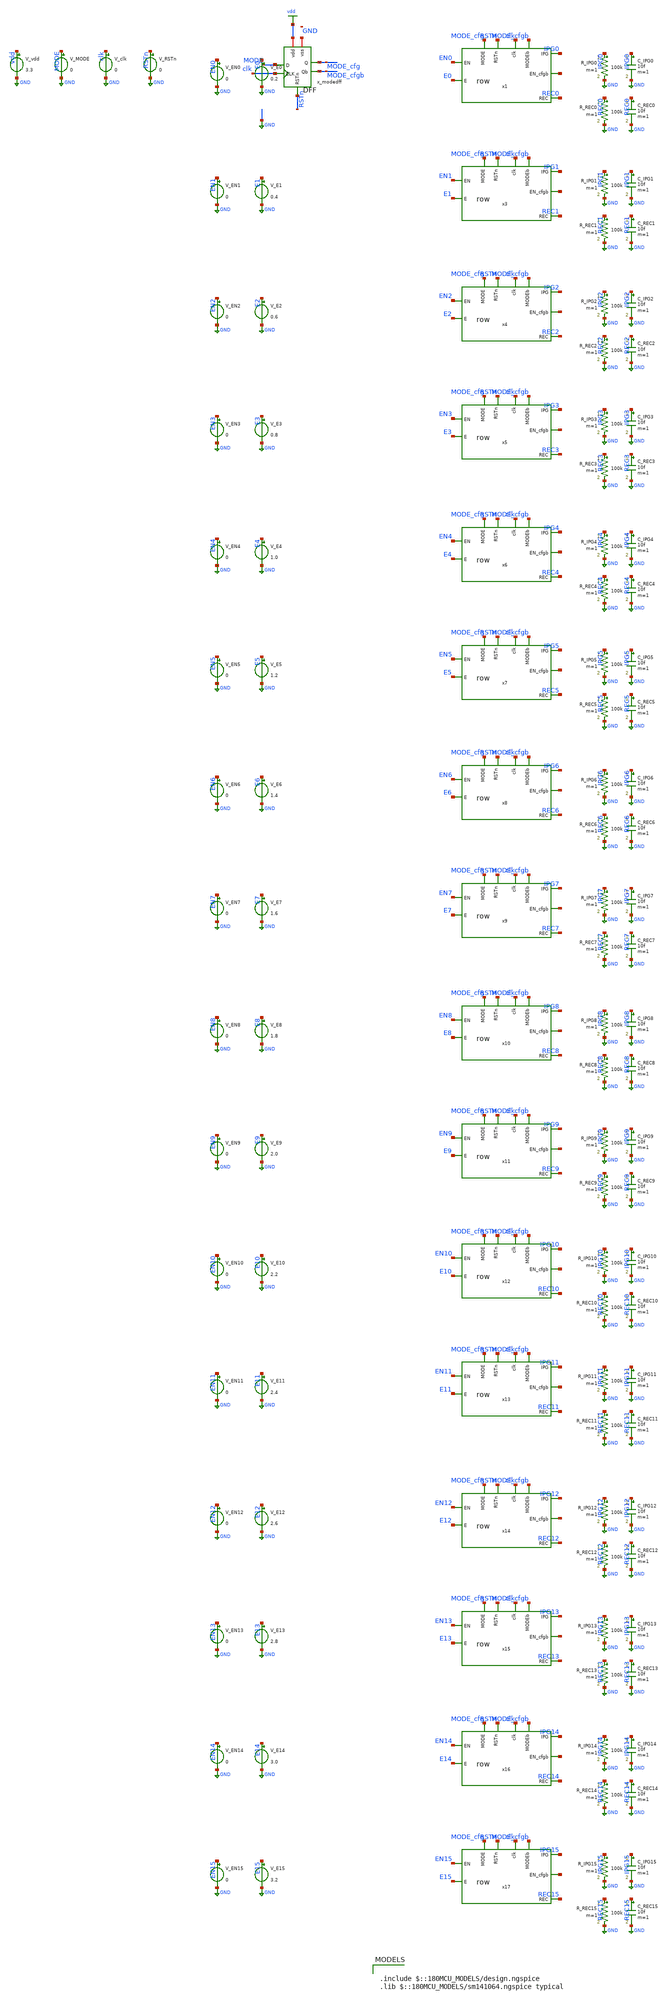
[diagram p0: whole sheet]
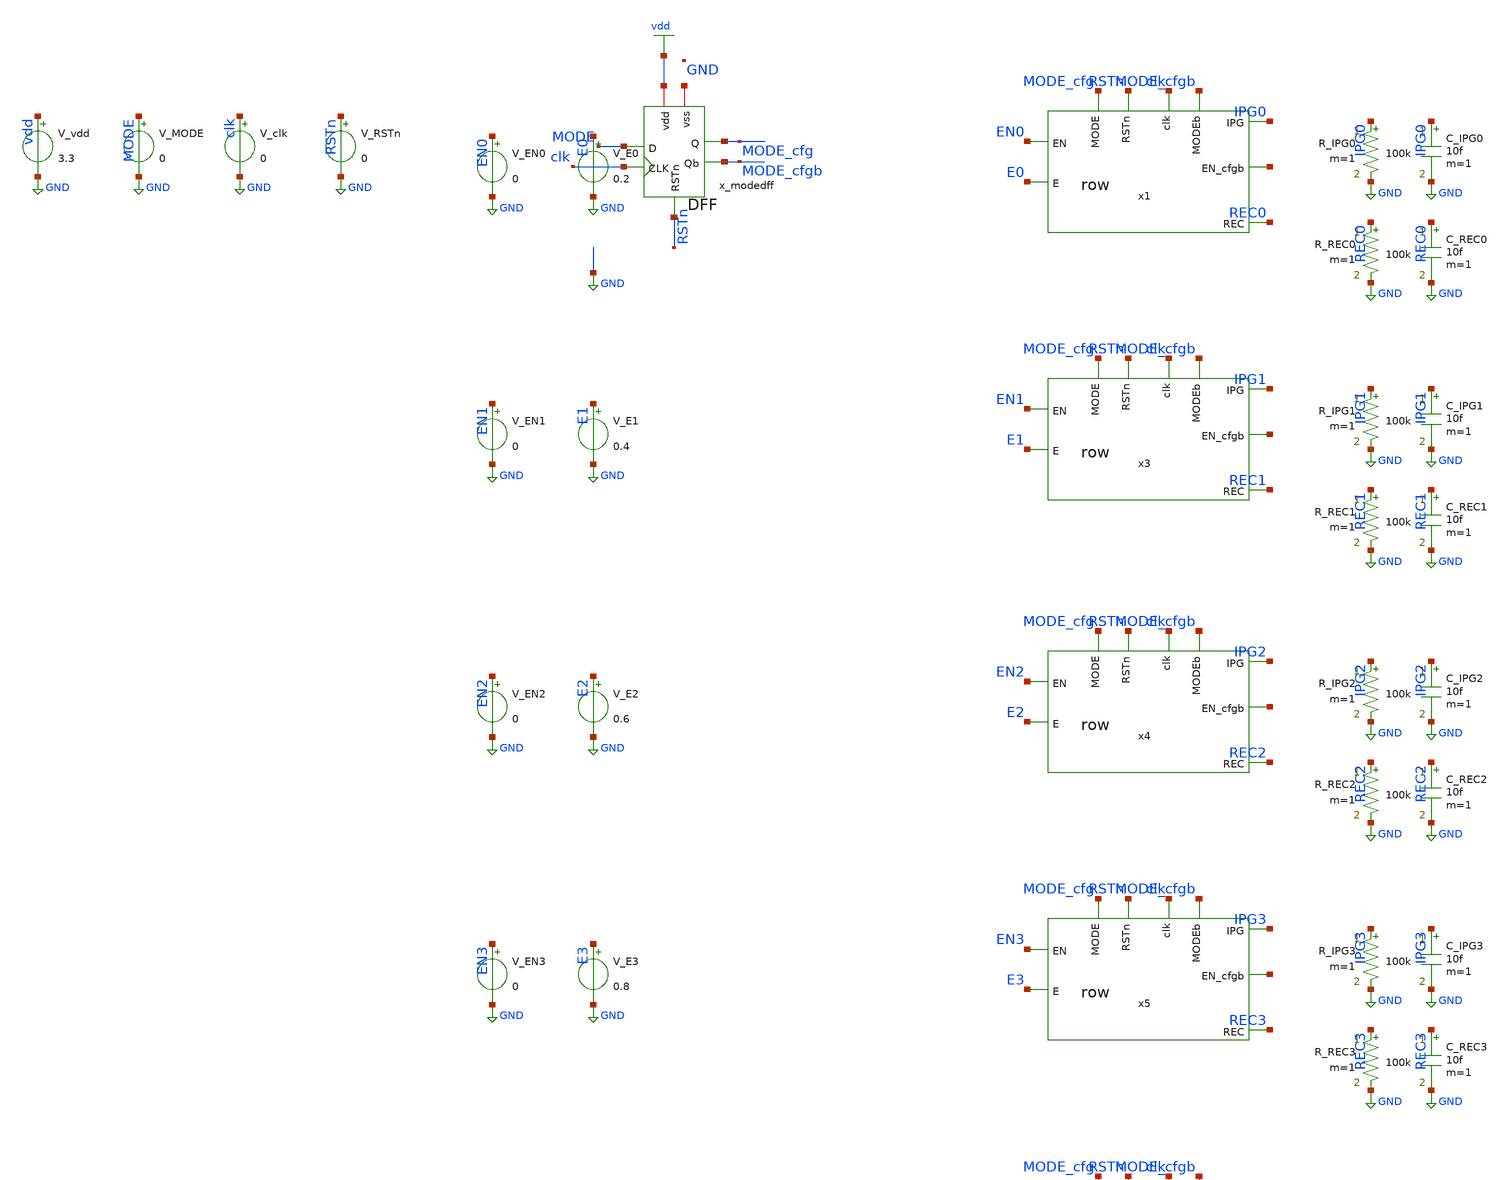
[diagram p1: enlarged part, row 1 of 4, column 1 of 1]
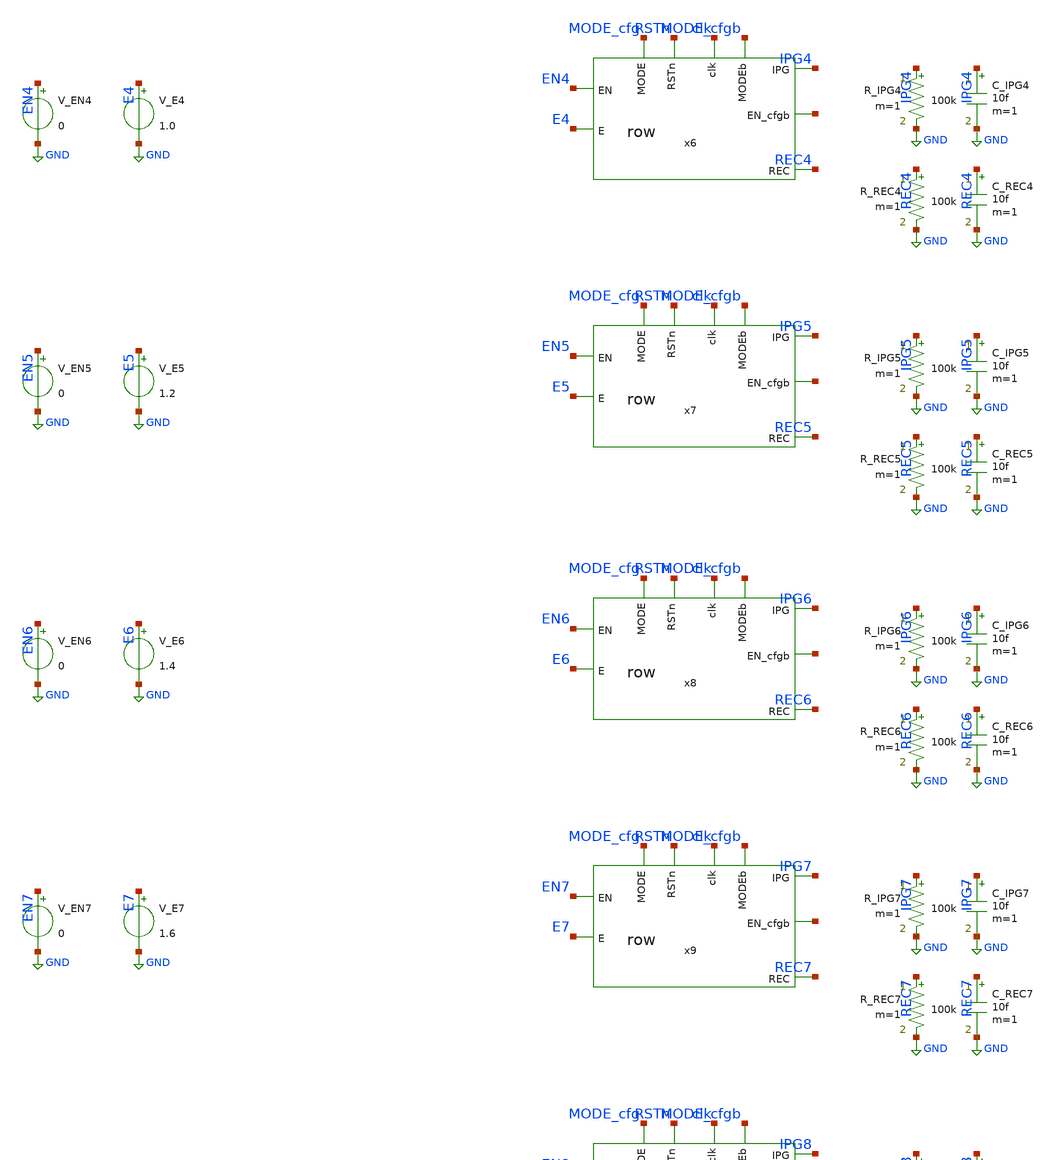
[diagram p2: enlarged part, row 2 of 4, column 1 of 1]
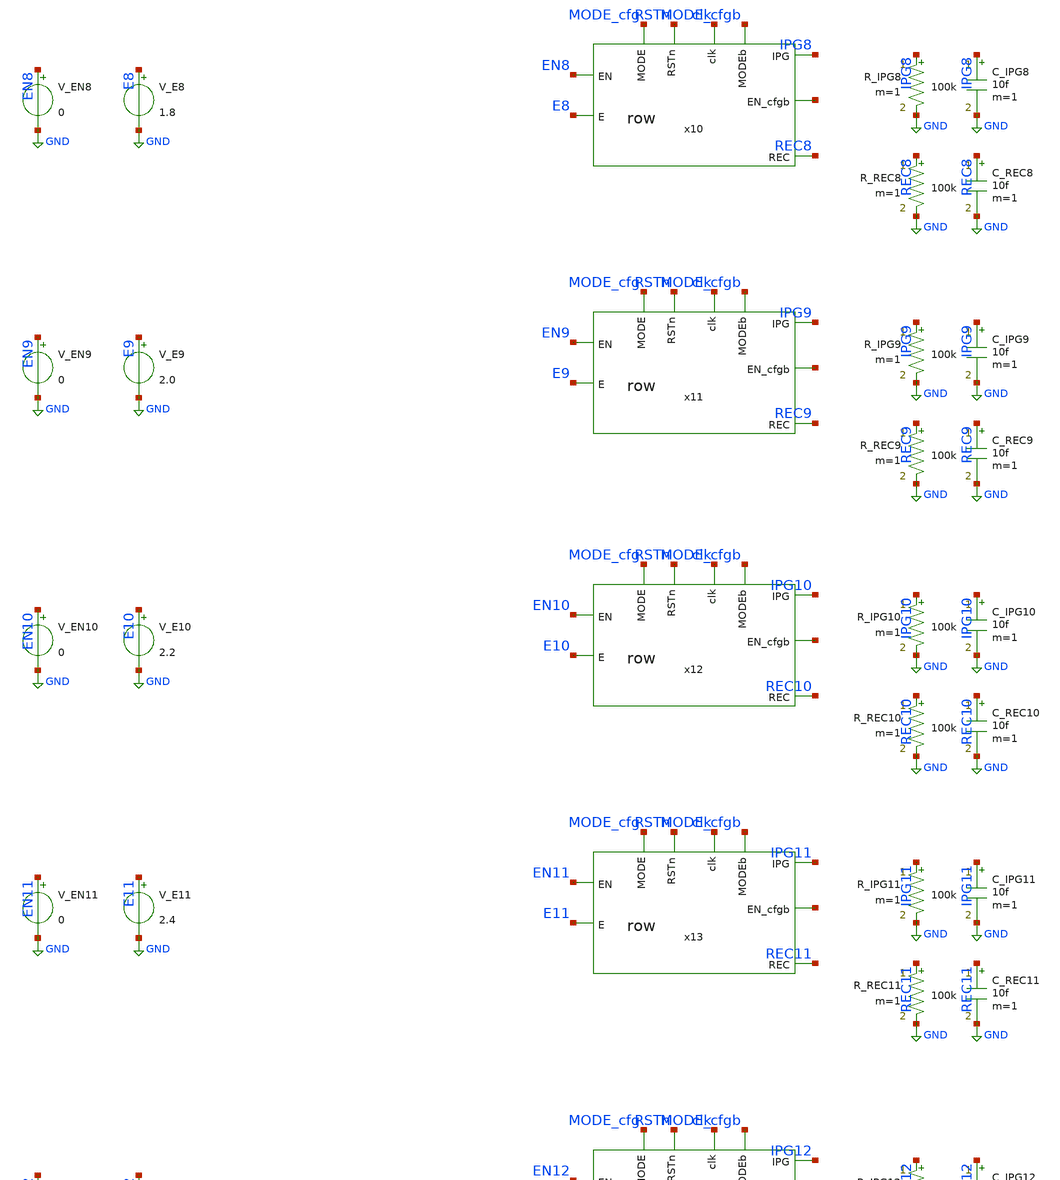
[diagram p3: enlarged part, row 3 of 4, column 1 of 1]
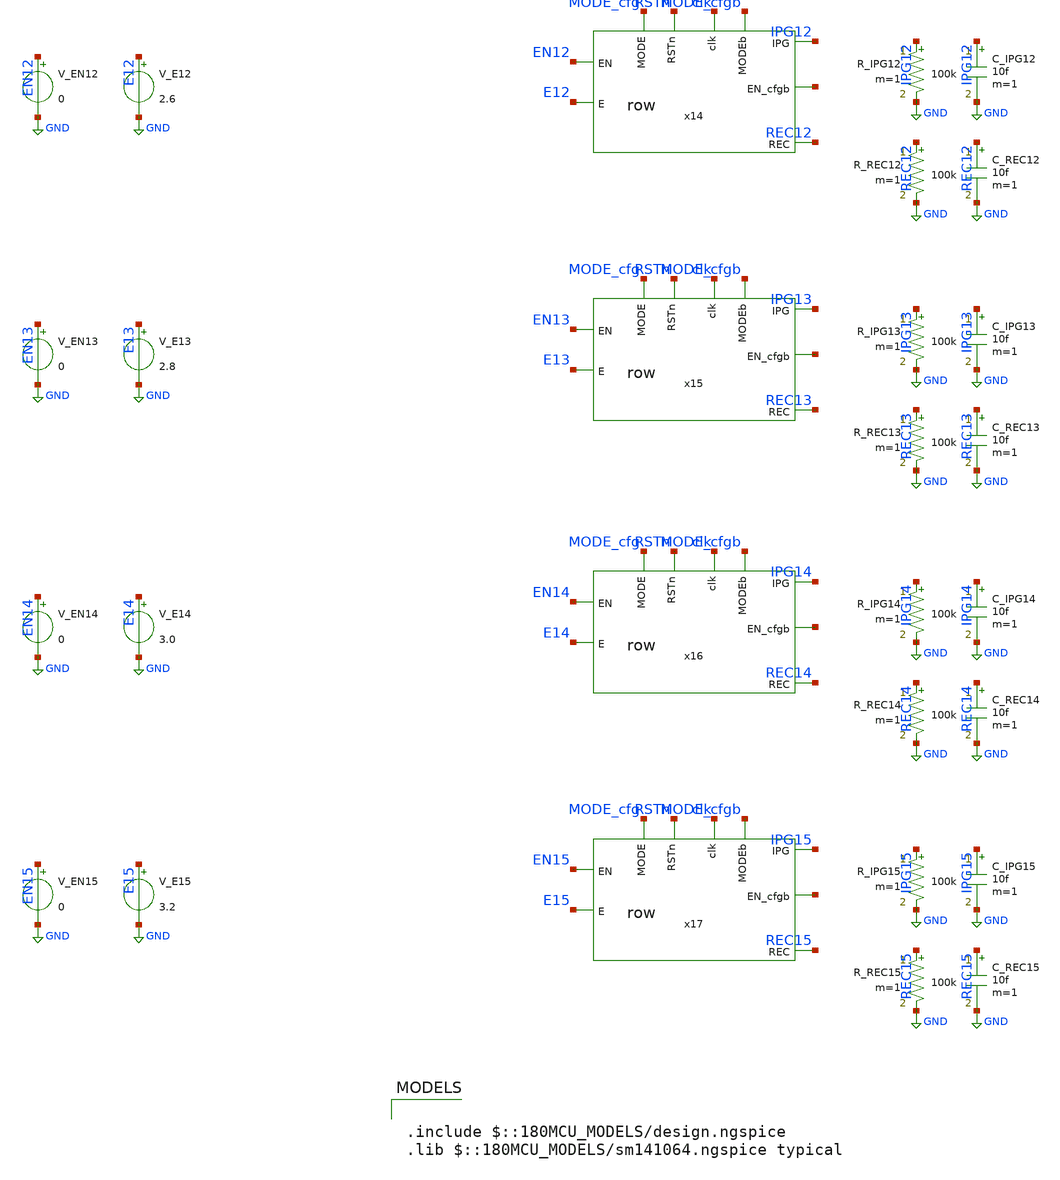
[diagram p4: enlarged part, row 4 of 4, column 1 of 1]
** sch_path: tb_full_allon.sch
**.subckt tb_full_allon
x_modedff vdd RSTn MODE MODE_cfg MODE_cfgb clk net1 DFF
V_RSTn RSTn GND 0
V_clk clk GND 0
V_MODE MODE GND 0
V_vdd vdd GND 3.3
x1 IPG0 MODE_cfgb EN0 net2 clk E0 MODE_cfg RSTn REC0 row
x3 IPG1 MODE_cfgb EN1 net3 clk E1 MODE_cfg RSTn REC1 row
x4 IPG2 MODE_cfgb EN2 net4 clk E2 MODE_cfg RSTn REC2 row
x5 IPG3 MODE_cfgb EN3 net5 clk E3 MODE_cfg RSTn REC3 row
x6 IPG4 MODE_cfgb EN4 net6 clk E4 MODE_cfg RSTn REC4 row
x7 IPG5 MODE_cfgb EN5 net7 clk E5 MODE_cfg RSTn REC5 row
x8 IPG6 MODE_cfgb EN6 net8 clk E6 MODE_cfg RSTn REC6 row
x9 IPG7 MODE_cfgb EN7 net9 clk E7 MODE_cfg RSTn REC7 row
x10 IPG8 MODE_cfgb EN8 net10 clk E8 MODE_cfg RSTn REC8 row
x11 IPG9 MODE_cfgb EN9 net11 clk E9 MODE_cfg RSTn REC9 row
x12 IPG10 MODE_cfgb EN10 net12 clk E10 MODE_cfg RSTn REC10 row
x13 IPG11 MODE_cfgb EN11 net13 clk E11 MODE_cfg RSTn REC11 row
x14 IPG12 MODE_cfgb EN12 net14 clk E12 MODE_cfg RSTn REC12 row
x15 IPG13 MODE_cfgb EN13 net15 clk E13 MODE_cfg RSTn REC13 row
x16 IPG14 MODE_cfgb EN14 net16 clk E14 MODE_cfg RSTn REC14 row
x17 IPG15 MODE_cfgb EN15 net17 clk E15 MODE_cfg RSTn REC15 row
V_EN0 EN0 GND 0
V_E0 E0 GND 0.2
V_EN1 EN1 GND 0
V_E1 E1 GND 0.4
V_EN2 EN2 GND 0
V_E2 E2 GND 0.6
V_EN3 EN3 GND 0
V_E3 E3 GND 0.8
V_EN4 EN4 GND 0
V_E4 E4 GND 1.0
V_EN5 EN5 GND 0
V_E5 E5 GND 1.2
V_EN6 EN6 GND 0
V_E6 E6 GND 1.4
V_EN7 EN7 GND 0
V_E7 E7 GND 1.6
V_EN8 EN8 GND 0
V_E8 E8 GND 1.8
V_EN9 EN9 GND 0
V_E9 E9 GND 2.0
V_EN10 EN10 GND 0
V_E10 E10 GND 2.2
V_EN11 EN11 GND 0
V_E11 E11 GND 2.4
V_EN12 EN12 GND 0
V_E12 E12 GND 2.6
V_EN13 EN13 GND 0
V_E13 E13 GND 2.8
V_EN14 EN14 GND 0
V_E14 E14 GND 3.0
V_EN15 EN15 GND 0
V_E15 E15 GND 3.2
R_IPG0 IPG0 GND 100k m=1
C_IPG0 IPG0 GND 10f m=1
R_REC0 REC0 GND 100k m=1
C_REC0 REC0 GND 10f m=1
R_IPG1 IPG1 GND 100k m=1
C_IPG1 IPG1 GND 10f m=1
R_REC1 REC1 GND 100k m=1
C_REC1 REC1 GND 10f m=1
R_IPG2 IPG2 GND 100k m=1
C_IPG2 IPG2 GND 10f m=1
R_REC2 REC2 GND 100k m=1
C_REC2 REC2 GND 10f m=1
R_IPG3 IPG3 GND 100k m=1
C_IPG3 IPG3 GND 10f m=1
R_REC3 REC3 GND 100k m=1
C_REC3 REC3 GND 10f m=1
R_IPG4 IPG4 GND 100k m=1
C_IPG4 IPG4 GND 10f m=1
R_REC4 REC4 GND 100k m=1
C_REC4 REC4 GND 10f m=1
R_IPG5 IPG5 GND 100k m=1
C_IPG5 IPG5 GND 10f m=1
R_REC5 REC5 GND 100k m=1
C_REC5 REC5 GND 10f m=1
R_IPG6 IPG6 GND 100k m=1
C_IPG6 IPG6 GND 10f m=1
R_REC6 REC6 GND 100k m=1
C_REC6 REC6 GND 10f m=1
R_IPG7 IPG7 GND 100k m=1
C_IPG7 IPG7 GND 10f m=1
R_REC7 REC7 GND 100k m=1
C_REC7 REC7 GND 10f m=1
R_IPG8 IPG8 GND 100k m=1
C_IPG8 IPG8 GND 10f m=1
R_REC8 REC8 GND 100k m=1
C_REC8 REC8 GND 10f m=1
R_IPG9 IPG9 GND 100k m=1
C_IPG9 IPG9 GND 10f m=1
R_REC9 REC9 GND 100k m=1
C_REC9 REC9 GND 10f m=1
R_IPG10 IPG10 GND 100k m=1
C_IPG10 IPG10 GND 10f m=1
R_REC10 REC10 GND 100k m=1
C_REC10 REC10 GND 10f m=1
R_IPG11 IPG11 GND 100k m=1
C_IPG11 IPG11 GND 10f m=1
R_REC11 REC11 GND 100k m=1
C_REC11 REC11 GND 10f m=1
R_IPG12 IPG12 GND 100k m=1
C_IPG12 IPG12 GND 10f m=1
R_REC12 REC12 GND 100k m=1
C_REC12 REC12 GND 10f m=1
R_IPG13 IPG13 GND 100k m=1
C_IPG13 IPG13 GND 10f m=1
R_REC13 REC13 GND 100k m=1
C_REC13 REC13 GND 10f m=1
R_IPG14 IPG14 GND 100k m=1
C_IPG14 IPG14 GND 10f m=1
R_REC14 REC14 GND 100k m=1
C_REC14 REC14 GND 10f m=1
R_IPG15 IPG15 GND 100k m=1
C_IPG15 IPG15 GND 10f m=1
R_REC15 REC15 GND 100k m=1
C_REC15 REC15 GND 10f m=1
**** begin user architecture code

.include $::180MCU_MODELS/design.ngspice
.lib $::180MCU_MODELS/sm141064.ngspice typical



.control
save all
alter @V_RSTn[PWL] = [ 0 0  100n 0  100.001n 3.3  10u 3.3 ]
alter @V_clk[PULSE] = [ 0 3.3 0 1n 1n 25n 50n ]
alter @V_MODE[PWL] = [ 0 0  500n 0  500.001n 3.3  10u 3.3 ]
alter @V_EN0[PWL]  = [ 0 0  150n 0  150.001n 3.3  10u 3.3 ]
alter @V_EN1[PWL]  = [ 0 0  150n 0  150.001n 3.3  10u 3.3 ]
alter @V_EN2[PWL]  = [ 0 0  150n 0  150.001n 3.3  10u 3.3 ]
alter @V_EN3[PWL]  = [ 0 0  150n 0  150.001n 3.3  10u 3.3 ]
alter @V_EN4[PWL]  = [ 0 0  150n 0  150.001n 3.3  10u 3.3 ]
alter @V_EN5[PWL]  = [ 0 0  150n 0  150.001n 3.3  10u 3.3 ]
alter @V_EN6[PWL]  = [ 0 0  150n 0  150.001n 3.3  10u 3.3 ]
alter @V_EN7[PWL]  = [ 0 0  150n 0  150.001n 3.3  10u 3.3 ]
alter @V_EN8[PWL]  = [ 0 0  150n 0  150.001n 3.3  10u 3.3 ]
alter @V_EN9[PWL]  = [ 0 0  150n 0  150.001n 3.3  10u 3.3 ]
alter @V_EN10[PWL] = [ 0 0  150n 0  150.001n 3.3  10u 3.3 ]
alter @V_EN11[PWL] = [ 0 0  150n 0  150.001n 3.3  10u 3.3 ]
alter @V_EN12[PWL] = [ 0 0  150n 0  150.001n 3.3  10u 3.3 ]
alter @V_EN13[PWL] = [ 0 0  150n 0  150.001n 3.3  10u 3.3 ]
alter @V_EN14[PWL] = [ 0 0  150n 0  150.001n 3.3  10u 3.3 ]
alter @V_EN15[PWL] = [ 0 0  150n 0  150.001n 3.3  10u 3.3 ]
tran 1n 800n
write tb_full_allon.raw
.endc


**** end user architecture code
**.ends

* expanding   symbol:  DFF/DFF.sym # of pins=7
** sym_path: DFF/DFF.sym
** sch_path: DFF/DFF.sch
.subckt DFF vdd RSTn D Q Qb CLK vss
*.ipin D
*.ipin CLK
*.ipin RSTn
*.opin Q
*.iopin vdd
*.iopin vss
*.opin Qb
XM1 net1 D net3 vss nfet_03v3 L=0.28u W=1u nf=1 ad='int((nf+1)/2) * W/nf * 0.18u' as='int((nf+2)/2) * W/nf * 0.18u'
+ pd='2*int((nf+1)/2) * (W/nf + 0.18u)' ps='2*int((nf+2)/2) * (W/nf + 0.18u)' nrd='0.18u / W' nrs='0.18u / W'
+ sa=0 sb=0 sd=0 m=1
XM2 net1 D net2 vdd pfet_03v3 L=0.28u W=1u nf=1 ad='int((nf+1)/2) * W/nf * 0.18u' as='int((nf+2)/2) * W/nf * 0.18u'
+ pd='2*int((nf+1)/2) * (W/nf + 0.18u)' ps='2*int((nf+2)/2) * (W/nf + 0.18u)' nrd='0.18u / W' nrs='0.18u / W'
+ sa=0 sb=0 sd=0 m=1
XM3 net2 c vdd vdd pfet_03v3 L=0.28u W=1u nf=1 ad='int((nf+1)/2) * W/nf * 0.18u' as='int((nf+2)/2) * W/nf * 0.18u'
+ pd='2*int((nf+1)/2) * (W/nf + 0.18u)' ps='2*int((nf+2)/2) * (W/nf + 0.18u)' nrd='0.18u / W' nrs='0.18u / W'
+ sa=0 sb=0 sd=0 m=1
XM4 net3 cbar vss vss nfet_03v3 L=0.28u W=1u nf=1 ad='int((nf+1)/2) * W/nf * 0.18u' as='int((nf+2)/2) * W/nf * 0.18u'
+ pd='2*int((nf+1)/2) * (W/nf + 0.18u)' ps='2*int((nf+2)/2) * (W/nf + 0.18u)' nrd='0.18u / W' nrs='0.18u / W'
+ sa=0 sb=0 sd=0 m=1
XM5 cbar CLK vss vss nfet_03v3 L=0.28u W=1u nf=1 ad='int((nf+1)/2) * W/nf * 0.18u' as='int((nf+2)/2) * W/nf * 0.18u'
+ pd='2*int((nf+1)/2) * (W/nf + 0.18u)' ps='2*int((nf+2)/2) * (W/nf + 0.18u)' nrd='0.18u / W' nrs='0.18u / W'
+ sa=0 sb=0 sd=0 m=1
XM6 cbar CLK vdd vdd pfet_03v3 L=0.28u W=1u nf=1 ad='int((nf+1)/2) * W/nf * 0.18u' as='int((nf+2)/2) * W/nf * 0.18u'
+ pd='2*int((nf+1)/2) * (W/nf + 0.18u)' ps='2*int((nf+2)/2) * (W/nf + 0.18u)' nrd='0.18u / W' nrs='0.18u / W'
+ sa=0 sb=0 sd=0 m=1
XM7 c cbar vss vss nfet_03v3 L=0.28u W=1u nf=1 ad='int((nf+1)/2) * W/nf * 0.18u' as='int((nf+2)/2) * W/nf * 0.18u'
+ pd='2*int((nf+1)/2) * (W/nf + 0.18u)' ps='2*int((nf+2)/2) * (W/nf + 0.18u)' nrd='0.18u / W' nrs='0.18u / W'
+ sa=0 sb=0 sd=0 m=1
XM8 c cbar vdd vdd pfet_03v3 L=0.28u W=1u nf=1 ad='int((nf+1)/2) * W/nf * 0.18u' as='int((nf+2)/2) * W/nf * 0.18u'
+ pd='2*int((nf+1)/2) * (W/nf + 0.18u)' ps='2*int((nf+2)/2) * (W/nf + 0.18u)' nrd='0.18u / W' nrs='0.18u / W'
+ sa=0 sb=0 sd=0 m=1
XM11 net5 RSTn net4 vss nfet_03v3 L=0.28u W=1u nf=1 ad='int((nf+1)/2) * W/nf * 0.18u' as='int((nf+2)/2) * W/nf * 0.18u'
+ pd='2*int((nf+1)/2) * (W/nf + 0.18u)' ps='2*int((nf+2)/2) * (W/nf + 0.18u)' nrd='0.18u / W' nrs='0.18u / W'
+ sa=0 sb=0 sd=0 m=1
XM12 net4 net6 vss vss nfet_03v3 L=0.28u W=1u nf=1 ad='int((nf+1)/2) * W/nf * 0.18u' as='int((nf+2)/2) * W/nf * 0.18u'
+ pd='2*int((nf+1)/2) * (W/nf + 0.18u)' ps='2*int((nf+2)/2) * (W/nf + 0.18u)' nrd='0.18u / W' nrs='0.18u / W'
+ sa=0 sb=0 sd=0 m=1
XM13 net5 RSTn vdd vdd pfet_03v3 L=0.28u W=1u nf=1 ad='int((nf+1)/2) * W/nf * 0.18u' as='int((nf+2)/2) * W/nf * 0.18u'
+ pd='2*int((nf+1)/2) * (W/nf + 0.18u)' ps='2*int((nf+2)/2) * (W/nf + 0.18u)' nrd='0.18u / W' nrs='0.18u / W'
+ sa=0 sb=0 sd=0 m=1
XM14 net5 net6 vdd vdd pfet_03v3 L=0.28u W=1u nf=1 ad='int((nf+1)/2) * W/nf * 0.18u' as='int((nf+2)/2) * W/nf * 0.18u'
+ pd='2*int((nf+1)/2) * (W/nf + 0.18u)' ps='2*int((nf+2)/2) * (W/nf + 0.18u)' nrd='0.18u / W' nrs='0.18u / W'
+ sa=0 sb=0 sd=0 m=1
XM15 net6 net1 vss vss nfet_03v3 L=0.28u W=1u nf=1 ad='int((nf+1)/2) * W/nf * 0.18u' as='int((nf+2)/2) * W/nf * 0.18u'
+ pd='2*int((nf+1)/2) * (W/nf + 0.18u)' ps='2*int((nf+2)/2) * (W/nf + 0.18u)' nrd='0.18u / W' nrs='0.18u / W'
+ sa=0 sb=0 sd=0 m=1
XM16 net6 net1 vdd vdd pfet_03v3 L=0.28u W=1u nf=1 ad='int((nf+1)/2) * W/nf * 0.18u' as='int((nf+2)/2) * W/nf * 0.18u'
+ pd='2*int((nf+1)/2) * (W/nf + 0.18u)' ps='2*int((nf+2)/2) * (W/nf + 0.18u)' nrd='0.18u / W' nrs='0.18u / W'
+ sa=0 sb=0 sd=0 m=1
XM21 net9 net7 net8 vss nfet_03v3 L=0.28u W=1u nf=1 ad='int((nf+1)/2) * W/nf * 0.18u' as='int((nf+2)/2) * W/nf * 0.18u'
+ pd='2*int((nf+1)/2) * (W/nf + 0.18u)' ps='2*int((nf+2)/2) * (W/nf + 0.18u)' nrd='0.18u / W' nrs='0.18u / W'
+ sa=0 sb=0 sd=0 m=1
XM22 net8 RSTn vss vss nfet_03v3 L=0.28u W=1u nf=1 ad='int((nf+1)/2) * W/nf * 0.18u' as='int((nf+2)/2) * W/nf * 0.18u'
+ pd='2*int((nf+1)/2) * (W/nf + 0.18u)' ps='2*int((nf+2)/2) * (W/nf + 0.18u)' nrd='0.18u / W' nrs='0.18u / W'
+ sa=0 sb=0 sd=0 m=1
XM23 net9 net7 vdd vdd pfet_03v3 L=0.28u W=1u nf=1 ad='int((nf+1)/2) * W/nf * 0.18u' as='int((nf+2)/2) * W/nf * 0.18u'
+ pd='2*int((nf+1)/2) * (W/nf + 0.18u)' ps='2*int((nf+2)/2) * (W/nf + 0.18u)' nrd='0.18u / W' nrs='0.18u / W'
+ sa=0 sb=0 sd=0 m=1
XM24 net9 RSTn vdd vdd pfet_03v3 L=0.28u W=1u nf=1 ad='int((nf+1)/2) * W/nf * 0.18u' as='int((nf+2)/2) * W/nf * 0.18u'
+ pd='2*int((nf+1)/2) * (W/nf + 0.18u)' ps='2*int((nf+2)/2) * (W/nf + 0.18u)' nrd='0.18u / W' nrs='0.18u / W'
+ sa=0 sb=0 sd=0 m=1
XM25 Q net9 vss vss nfet_03v3 L=0.28u W=1u nf=1 ad='int((nf+1)/2) * W/nf * 0.18u' as='int((nf+2)/2) * W/nf * 0.18u'
+ pd='2*int((nf+1)/2) * (W/nf + 0.18u)' ps='2*int((nf+2)/2) * (W/nf + 0.18u)' nrd='0.18u / W' nrs='0.18u / W'
+ sa=0 sb=0 sd=0 m=1
XM26 Q net9 vdd vdd pfet_03v3 L=0.28u W=1u nf=1 ad='int((nf+1)/2) * W/nf * 0.18u' as='int((nf+2)/2) * W/nf * 0.18u'
+ pd='2*int((nf+1)/2) * (W/nf + 0.18u)' ps='2*int((nf+2)/2) * (W/nf + 0.18u)' nrd='0.18u / W' nrs='0.18u / W'
+ sa=0 sb=0 sd=0 m=1
XM19 net7 net9 net11 vss nfet_03v3 L=0.28u W=1u nf=1 ad='int((nf+1)/2) * W/nf * 0.18u' as='int((nf+2)/2) * W/nf * 0.18u'
+ pd='2*int((nf+1)/2) * (W/nf + 0.18u)' ps='2*int((nf+2)/2) * (W/nf + 0.18u)' nrd='0.18u / W' nrs='0.18u / W'
+ sa=0 sb=0 sd=0 m=1
XM20 net7 net9 net10 vdd pfet_03v3 L=0.28u W=1u nf=1 ad='int((nf+1)/2) * W/nf * 0.18u' as='int((nf+2)/2) * W/nf * 0.18u'
+ pd='2*int((nf+1)/2) * (W/nf + 0.18u)' ps='2*int((nf+2)/2) * (W/nf + 0.18u)' nrd='0.18u / W' nrs='0.18u / W'
+ sa=0 sb=0 sd=0 m=1
XM31 net10 c vdd vdd pfet_03v3 L=0.28u W=1u nf=1 ad='int((nf+1)/2) * W/nf * 0.18u' as='int((nf+2)/2) * W/nf * 0.18u'
+ pd='2*int((nf+1)/2) * (W/nf + 0.18u)' ps='2*int((nf+2)/2) * (W/nf + 0.18u)' nrd='0.18u / W' nrs='0.18u / W'
+ sa=0 sb=0 sd=0 m=1
XM32 net11 cbar vss vss nfet_03v3 L=0.28u W=1u nf=1 ad='int((nf+1)/2) * W/nf * 0.18u' as='int((nf+2)/2) * W/nf * 0.18u'
+ pd='2*int((nf+1)/2) * (W/nf + 0.18u)' ps='2*int((nf+2)/2) * (W/nf + 0.18u)' nrd='0.18u / W' nrs='0.18u / W'
+ sa=0 sb=0 sd=0 m=1
XM35 net12 net9 vss vss nfet_03v3 L=0.28u W=1u nf=1 ad='int((nf+1)/2) * W/nf * 0.18u' as='int((nf+2)/2) * W/nf * 0.18u'
+ pd='2*int((nf+1)/2) * (W/nf + 0.18u)' ps='2*int((nf+2)/2) * (W/nf + 0.18u)' nrd='0.18u / W' nrs='0.18u / W'
+ sa=0 sb=0 sd=0 m=1
XM36 net12 net9 vdd vdd pfet_03v3 L=0.28u W=1u nf=1 ad='int((nf+1)/2) * W/nf * 0.18u' as='int((nf+2)/2) * W/nf * 0.18u'
+ pd='2*int((nf+1)/2) * (W/nf + 0.18u)' ps='2*int((nf+2)/2) * (W/nf + 0.18u)' nrd='0.18u / W' nrs='0.18u / W'
+ sa=0 sb=0 sd=0 m=1
XM37 Qb net12 vss vss nfet_03v3 L=0.28u W=1u nf=1 ad='int((nf+1)/2) * W/nf * 0.18u' as='int((nf+2)/2) * W/nf * 0.18u'
+ pd='2*int((nf+1)/2) * (W/nf + 0.18u)' ps='2*int((nf+2)/2) * (W/nf + 0.18u)' nrd='0.18u / W' nrs='0.18u / W'
+ sa=0 sb=0 sd=0 m=1
XM38 Qb net12 vdd vdd pfet_03v3 L=0.28u W=1u nf=1 ad='int((nf+1)/2) * W/nf * 0.18u' as='int((nf+2)/2) * W/nf * 0.18u'
+ pd='2*int((nf+1)/2) * (W/nf + 0.18u)' ps='2*int((nf+2)/2) * (W/nf + 0.18u)' nrd='0.18u / W' nrs='0.18u / W'
+ sa=0 sb=0 sd=0 m=1
XM9 net1 c net5 vss nfet_03v3 L=0.28u W=1u nf=1 ad='int((nf+1)/2) * W/nf * 0.18u' as='int((nf+2)/2) * W/nf * 0.18u'
+ pd='2*int((nf+1)/2) * (W/nf + 0.18u)' ps='2*int((nf+2)/2) * (W/nf + 0.18u)' nrd='0.18u / W' nrs='0.18u / W'
+ sa=0 sb=0 sd=0 m=1
XM10 net1 cbar net5 vdd pfet_03v3 L=0.28u W=1u nf=1 ad='int((nf+1)/2) * W/nf * 0.18u' as='int((nf+2)/2) * W/nf * 0.18u'
+ pd='2*int((nf+1)/2) * (W/nf + 0.18u)' ps='2*int((nf+2)/2) * (W/nf + 0.18u)' nrd='0.18u / W' nrs='0.18u / W'
+ sa=0 sb=0 sd=0 m=1
XM17 net6 c net7 vss nfet_03v3 L=0.28u W=1u nf=1 ad='int((nf+1)/2) * W/nf * 0.18u' as='int((nf+2)/2) * W/nf * 0.18u'
+ pd='2*int((nf+1)/2) * (W/nf + 0.18u)' ps='2*int((nf+2)/2) * (W/nf + 0.18u)' nrd='0.18u / W' nrs='0.18u / W'
+ sa=0 sb=0 sd=0 m=1
XM18 net6 cbar net7 vdd pfet_03v3 L=0.28u W=1u nf=1 ad='int((nf+1)/2) * W/nf * 0.18u' as='int((nf+2)/2) * W/nf * 0.18u'
+ pd='2*int((nf+1)/2) * (W/nf + 0.18u)' ps='2*int((nf+2)/2) * (W/nf + 0.18u)' nrd='0.18u / W' nrs='0.18u / W'
+ sa=0 sb=0 sd=0 m=1
.ends


* expanding   symbol:  row.sym # of pins=9
** sym_path: row.sym
** sch_path: row.sch
.subckt row IPG MODEb EN EN_cfgb clk E MODE RSTn REC
*.ipin EN
*.ipin clk
*.ipin MODEb
*.ipin MODE
*.ipin E
*.opin IPG
*.opin REC
*.ipin RSTn
*.opin EN_cfgb
x1 EN_cfg SW_IPG MODEb AND
x2 vdd RSTn EN EN_cfg EN_cfgb clk GND DFF
x3 IPG SW_IPG SW_IPGb E TGATE
x4 EN_cfg SW_REC MODE AND
x6 REC SW_REC SW_RECb E TGATE
x5 SW_IPGb SW_IPG INV
x7 SW_RECb SW_REC INV
.ends


* expanding   symbol:  AND/AND.sym # of pins=3
** sym_path: AND/AND.sym
** sch_path: AND/AND.sch
.subckt AND IN0 OUT IN1
*.opin OUT
*.ipin IN0
*.ipin IN1
XM1 net1 IN0 net2 GND nfet_03v3 L=0.28u W=1u nf=1 ad='int((nf+1)/2) * W/nf * 0.18u' as='int((nf+2)/2) * W/nf * 0.18u'
+ pd='2*int((nf+1)/2) * (W/nf + 0.18u)' ps='2*int((nf+2)/2) * (W/nf + 0.18u)' nrd='0.18u / W' nrs='0.18u / W'
+ sa=0 sb=0 sd=0 m=1
XM2 net2 IN1 GND GND nfet_03v3 L=0.28u W=1u nf=1 ad='int((nf+1)/2) * W/nf * 0.18u' as='int((nf+2)/2) * W/nf * 0.18u'
+ pd='2*int((nf+1)/2) * (W/nf + 0.18u)' ps='2*int((nf+2)/2) * (W/nf + 0.18u)' nrd='0.18u / W' nrs='0.18u / W'
+ sa=0 sb=0 sd=0 m=1
XM3 net1 IN0 vdd vdd pfet_03v3 L=0.28u W=1u nf=1 ad='int((nf+1)/2) * W/nf * 0.18u' as='int((nf+2)/2) * W/nf * 0.18u'
+ pd='2*int((nf+1)/2) * (W/nf + 0.18u)' ps='2*int((nf+2)/2) * (W/nf + 0.18u)' nrd='0.18u / W' nrs='0.18u / W'
+ sa=0 sb=0 sd=0 m=1
XM4 net1 IN1 vdd vdd pfet_03v3 L=0.28u W=1u nf=1 ad='int((nf+1)/2) * W/nf * 0.18u' as='int((nf+2)/2) * W/nf * 0.18u'
+ pd='2*int((nf+1)/2) * (W/nf + 0.18u)' ps='2*int((nf+2)/2) * (W/nf + 0.18u)' nrd='0.18u / W' nrs='0.18u / W'
+ sa=0 sb=0 sd=0 m=1
x1 OUT net1 INV
.ends


* expanding   symbol:  TGATE/TGATE.sym # of pins=4
** sym_path: TGATE/TGATE.sym
** sch_path: TGATE/TGATE.sch
.subckt TGATE out c cbar in
*.ipin in
*.opin out
*.ipin cbar
*.ipin c
XM1 out cbar in VDD pfet_03v3 L=0.28u W=1u nf=1 ad='int((nf+1)/2) * W/nf * 0.18u' as='int((nf+2)/2) * W/nf * 0.18u'
+ pd='2*int((nf+1)/2) * (W/nf + 0.18u)' ps='2*int((nf+2)/2) * (W/nf + 0.18u)' nrd='0.18u / W' nrs='0.18u / W'
+ sa=0 sb=0 sd=0 m=1
XM2 out c in GND nfet_03v3 L=0.28u W=1u nf=1 ad='int((nf+1)/2) * W/nf * 0.18u' as='int((nf+2)/2) * W/nf * 0.18u'
+ pd='2*int((nf+1)/2) * (W/nf + 0.18u)' ps='2*int((nf+2)/2) * (W/nf + 0.18u)' nrd='0.18u / W' nrs='0.18u / W'
+ sa=0 sb=0 sd=0 m=1
.ends


* expanding   symbol:  AND/INV.sym # of pins=2
** sym_path: AND/INV.sym
** sch_path: AND/INV.sch
.subckt INV OUT IN
*.ipin IN
*.opin OUT
XM1 OUT IN VDD VDD pfet_03v3 L=0.28u W=1u nf=1 ad='int((nf+1)/2) * W/nf * 0.18u' as='int((nf+2)/2) * W/nf * 0.18u'
+ pd='2*int((nf+1)/2) * (W/nf + 0.18u)' ps='2*int((nf+2)/2) * (W/nf + 0.18u)' nrd='0.18u / W' nrs='0.18u / W'
+ sa=0 sb=0 sd=0 m=1
XM2 OUT IN GND GND nfet_03v3 L=0.28u W=0.5u nf=1 ad='int((nf+1)/2) * W/nf * 0.18u' as='int((nf+2)/2) * W/nf * 0.18u'
+ pd='2*int((nf+1)/2) * (W/nf + 0.18u)' ps='2*int((nf+2)/2) * (W/nf + 0.18u)' nrd='0.18u / W' nrs='0.18u / W'
+ sa=0 sb=0 sd=0 m=1
.ends

.GLOBAL GND
.GLOBAL vdd
.GLOBAL VDD
.end
